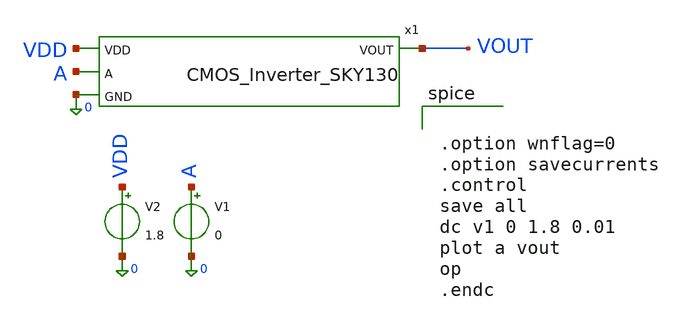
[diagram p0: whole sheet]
** sch_path: CMOS_Inverter_SKY130_testbench.sch
**.subckt CMOS_Inverter_SKY130_testbench
x1 VDD A VOUT 0 CMOS_Inverter_SKY130
V1 A 0 0
V2 VDD 0 1.8
**** begin user architecture code


.option wnflag=0
.option savecurrents
.control
save all
dc v1 0 1.8 0.01
plot a vout
op
.endc


 .lib /foss/pdks/sky130A/libs.tech/ngspice/sky130.lib.spice tt
.param mc_mm_switch=0
.param mc_pr_switch=1

**** end user architecture code
**.ends

* expanding   symbol:  CMOS_Inverter_SKY130.sym # of pins=4
** sym_path: CMOS_Inverter_SKY130.sym
** sch_path: CMOS_Inverter_SKY130.sch
.subckt CMOS_Inverter_SKY130 VDD A VOUT GND
*.ipin A
*.ipin VDD
*.ipin GND
*.opin VOUT
XM18 VOUT A GND GND sky130_fd_pr__nfet_01v8 L=0.15 W=7 nf=1 ad='int((nf+1)/2) * W/nf * 0.29' as='int((nf+2)/2) * W/nf * 0.29'
+ pd='2*int((nf+1)/2) * (W/nf + 0.29)' ps='2*int((nf+2)/2) * (W/nf + 0.29)' nrd='0.29 / W' nrs='0.29 / W'
+ sa=0 sb=0 sd=0 mult=1 m=1
XT1 VOUT A VDD VDD sky130_fd_pr__pfet_01v8 L=0.15 W=21 nf=1 ad='int((1 + 1)/2) * 21 / 1 * 0.29' as='int((1 + 2)/2) * 21 / 1 * 0.29'
+ pd='2*int((1 + 1)/2) * (21 / 1 + 0.29)' ps='2*int((1 + 2)/2) * (21 / 1 + 0.29)' nrd='0.29 / 21 ' nrs='0.29 / 21 '
+ sa=0 sb=0 sd=0 mult=1 m=1
.ends

.end
